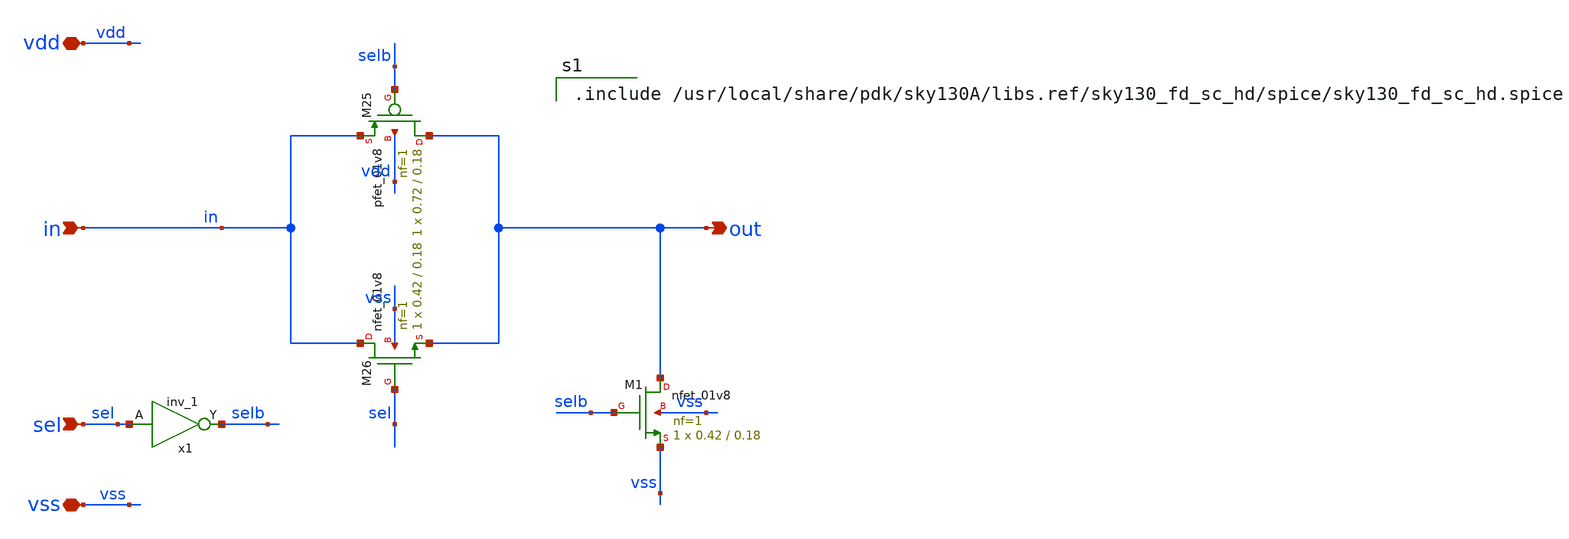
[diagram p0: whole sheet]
** sch_path: xschem/3-stage_cs-vco_dp9/vco_switch_n.sch
**.subckt vco_switch_n in sel out vss vdd
*.ipin in
*.ipin sel
*.opin out
*.iopin vss
*.iopin vdd
XM26 in sel out vss sky130_fd_pr__nfet_01v8 L=0.18 W=0.42 nf=1 ad='int((nf+1)/2) * W/nf * 0.29' as='int((nf+2)/2) * W/nf * 0.29'
+ pd='2*int((nf+1)/2) * (W/nf + 0.29)' ps='2*int((nf+2)/2) * (W/nf + 0.29)' nrd='0.29 / W' nrs='0.29 / W'
+ sa=0 sb=0 sd=0 mult=1 m=1
XM25 out selb in vdd sky130_fd_pr__pfet_01v8 L=0.18 W=0.72 nf=1 ad='int((nf+1)/2) * W/nf * 0.29' as='int((nf+2)/2) * W/nf * 0.29'
+ pd='2*int((nf+1)/2) * (W/nf + 0.29)' ps='2*int((nf+2)/2) * (W/nf + 0.29)' nrd='0.29 / W' nrs='0.29 / W'
+ sa=0 sb=0 sd=0 mult=1 m=1
XM1 out selb vss vss sky130_fd_pr__nfet_01v8 L=0.18 W=0.42 nf=1 ad='int((nf+1)/2) * W/nf * 0.29' as='int((nf+2)/2) * W/nf * 0.29'
+ pd='2*int((nf+1)/2) * (W/nf + 0.29)' ps='2*int((nf+2)/2) * (W/nf + 0.29)' nrd='0.29 / W' nrs='0.29 / W'
+ sa=0 sb=0 sd=0 mult=1 m=1
x1 sel vss vss vdd vdd selb sky130_fd_sc_hd__inv_1
**** begin user architecture code

.include /usr/local/share/pdk/sky130A/libs.ref/sky130_fd_sc_hd/spice/sky130_fd_sc_hd.spice

**** end user architecture code
**.ends
.end
